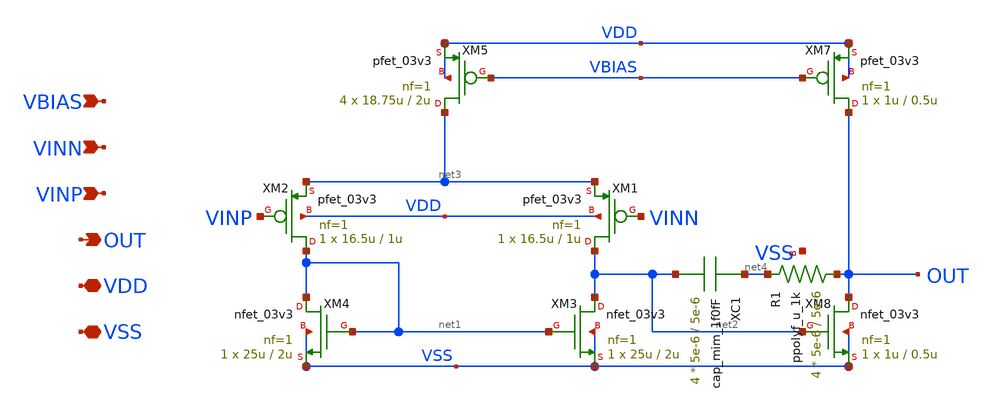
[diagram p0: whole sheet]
** sch_path: designs/libs/core_p-ota/pmos-ota/pmos-ota.sch
**.subckt pmos-ota VINN VINP OUT VDD VSS VBIAS
*.ipin VINN
*.ipin VINP
*.opin OUT
*.iopin VDD
*.iopin VSS
*.ipin VBIAS
XM1 net2 VINN net3 VDD pfet_03v3 L=1u W=16.5u nf=1 ad='int((nf+1)/2) * W/nf * 0.18u' as='int((nf+2)/2) * W/nf * 0.18u'
+ pd='2*int((nf+1)/2) * (W/nf + 0.18u)' ps='2*int((nf+2)/2) * (W/nf + 0.18u)' nrd='0.18u / W' nrs='0.18u / W'
+ sa=0 sb=0 sd=0 m=1
XM2 net1 VINP net3 VDD pfet_03v3 L=1u W=16.5u nf=1 ad='int((nf+1)/2) * W/nf * 0.18u' as='int((nf+2)/2) * W/nf * 0.18u'
+ pd='2*int((nf+1)/2) * (W/nf + 0.18u)' ps='2*int((nf+2)/2) * (W/nf + 0.18u)' nrd='0.18u / W' nrs='0.18u / W'
+ sa=0 sb=0 sd=0 m=1
XM3 net2 net1 VSS VSS nfet_03v3 L=2u W=25u nf=1 ad='int((nf+1)/2) * W/nf * 0.18u' as='int((nf+2)/2) * W/nf * 0.18u'
+ pd='2*int((nf+1)/2) * (W/nf + 0.18u)' ps='2*int((nf+2)/2) * (W/nf + 0.18u)' nrd='0.18u / W' nrs='0.18u / W'
+ sa=0 sb=0 sd=0 m=1
XM4 net1 net1 VSS VSS nfet_03v3 L=2u W=25u nf=1 ad='int((nf+1)/2) * W/nf * 0.18u' as='int((nf+2)/2) * W/nf * 0.18u'
+ pd='2*int((nf+1)/2) * (W/nf + 0.18u)' ps='2*int((nf+2)/2) * (W/nf + 0.18u)' nrd='0.18u / W' nrs='0.18u / W'
+ sa=0 sb=0 sd=0 m=1
XM5 net3 VBIAS VDD VDD pfet_03v3 L=2u W=18.75u nf=1 ad='int((nf+1)/2) * W/nf * 0.18u' as='int((nf+2)/2) * W/nf * 0.18u'
+ pd='2*int((nf+1)/2) * (W/nf + 0.18u)' ps='2*int((nf+2)/2) * (W/nf + 0.18u)' nrd='0.18u / W' nrs='0.18u / W'
+ sa=0 sb=0 sd=0 m=4
XM7 OUT VBIAS VDD VDD pfet_03v3 L=0.5u W=1u nf=1 ad='int((nf+1)/2) * W/nf * 0.18u' as='int((nf+2)/2) * W/nf * 0.18u'
+ pd='2*int((nf+1)/2) * (W/nf + 0.18u)' ps='2*int((nf+2)/2) * (W/nf + 0.18u)' nrd='0.18u / W' nrs='0.18u / W'
+ sa=0 sb=0 sd=0 m=1
XM8 OUT net2 VSS VSS nfet_03v3 L=0.5u W=1u nf=1 ad='int((nf+1)/2) * W/nf * 0.18u' as='int((nf+2)/2) * W/nf * 0.18u'
+ pd='2*int((nf+1)/2) * (W/nf + 0.18u)' ps='2*int((nf+2)/2) * (W/nf + 0.18u)' nrd='0.18u / W' nrs='0.18u / W'
+ sa=0 sb=0 sd=0 m=1
XC1 net4 net2 cap_mim_1f0fF c_width=5e-6 c_length=5e-6 m=4
XR1 OUT net4 VSS ppolyf_u_1k r_width=5e-6 r_length=5e-6 m=4
**.ends
.end
